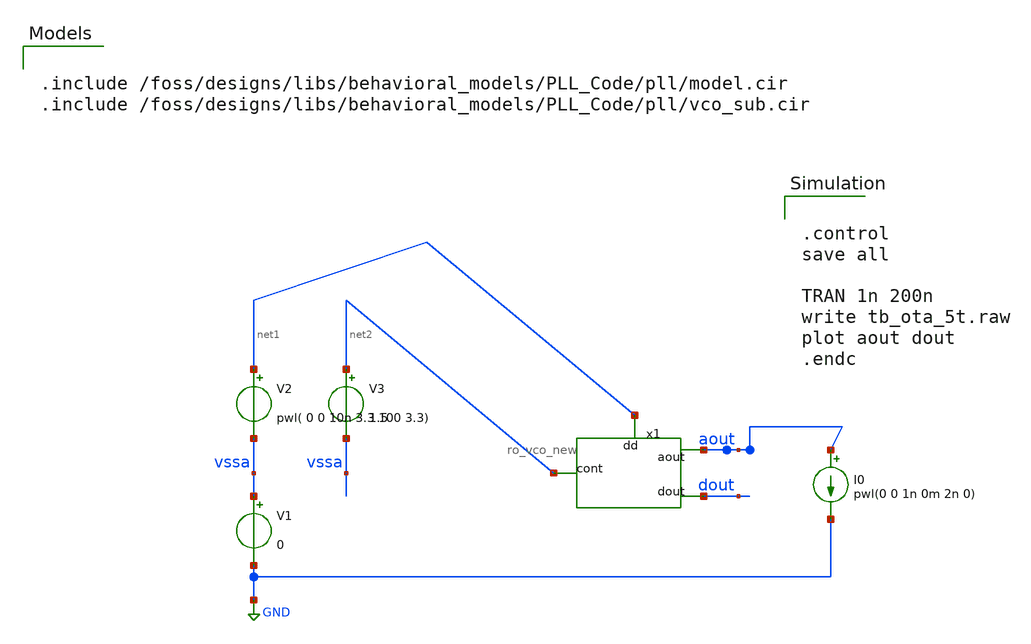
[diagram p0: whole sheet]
** sch_path: designs/libs/tb_analog/tb_PLL_behavioral_models/tb_ro_vco.sch
**.subckt tb_ro_vco
V1 vssa GND 0
V2 net1 vssa pwl( 0 0 10n 3.3 100 3.3)
V3 net2 vssa 1.5
x1 aout dout net2 net1 ro_vco_new
I0 aout GND pwl(0 0 1n 0m 2n 0)
**** begin user architecture code


.control
save all

TRAN 1n 200n
write tb_ota_5t.raw
plot aout dout
.endc



.include /foss/designs/libs/behavioral_models/PLL_Code/pll/model.cir
.include /foss/designs/libs/behavioral_models/PLL_Code/pll/vco_sub.cir

**** end user architecture code
**.ends
.GLOBAL GND
.end
